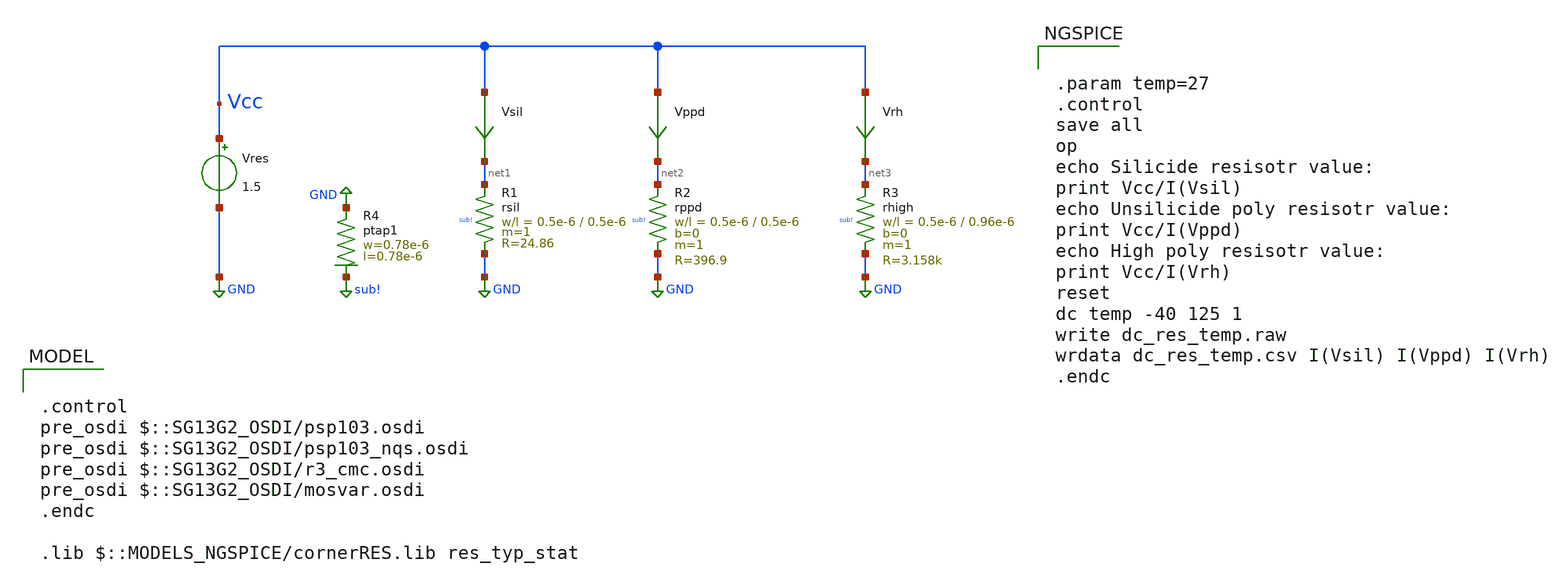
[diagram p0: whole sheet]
** sch_path: ihp-sg13g2/xschem_libs/sg13g2_tests/dc_res_temp/schematic/dc_res_temp.sch
* Copyright 2023 IHP PDK Authors
**.subckt dc_res_temp
Vres Vcc GND 1.5
Vsil Vcc net1 0
.save i(vsil)
Vppd Vcc net2 0
.save i(vppd)
Vrh Vcc net3 0
.save i(vrh)
XR4 GND sub! ptap1 R=262.8 w=0.78e-6 l=0.78e-6
XR1 net1 GND sub! rsil w=0.5e-6 l=0.5e-6 m=1 mm_ok=1
XR3 net3 GND sub! rhigh w=0.5e-6 l=0.96e-6 m=1 b=0 mm_ok=1
XR2 net2 GND sub! rppd w=0.5e-6 l=0.5e-6 m=1 b=0 mm_ok=1
**** begin user architecture code

.control
pre_osdi $::SG13G2_OSDI/psp103.osdi
pre_osdi $::SG13G2_OSDI/psp103_nqs.osdi
pre_osdi $::SG13G2_OSDI/r3_cmc.osdi
pre_osdi $::SG13G2_OSDI/mosvar.osdi
.endc

.lib $::MODELS_NGSPICE/cornerRES.lib res_typ_stat



.param temp=27
.control
save all
op
echo Silicide resisotr value:
print Vcc/I(Vsil)
echo Unsilicide poly resisotr value:
print Vcc/I(Vppd)
echo High poly resisotr value:
print Vcc/I(Vrh)
reset
dc temp -40 125 1
write dc_res_temp.raw
wrdata dc_res_temp.csv I(Vsil) I(Vppd) I(Vrh)
.endc


**** end user architecture code
**.ends
.GLOBAL GND
.GLOBAL sub!
.end
